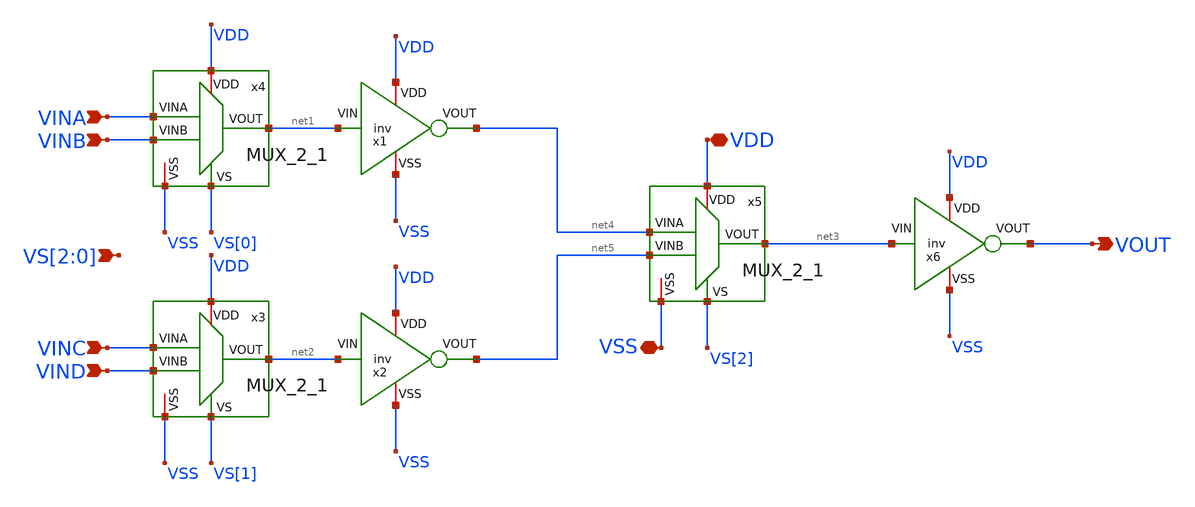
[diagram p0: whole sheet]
** sch_path: Custom_std_cells/MUX_4_1.sch
**.subckt MUX_4_1 VOUT VDD VSS VINA VINB VINC VIND VS[2],VS[1],VS[0]
*.opin VOUT
*.iopin VDD
*.iopin VSS
*.ipin VINA
*.ipin VINB
*.ipin VINC
*.ipin VIND
*.ipin VS[2],VS[1],VS[0]
x3 VDD VINC net2 VS[1] VIND VSS MUX_2_1
x4 VDD VINA net1 VS[0] VINB VSS MUX_2_1
x5 VDD net4 net3 VS[2] net5 VSS MUX_2_1
x1 VDD net4 net1 VSS inv
x2 VDD net5 net2 VSS inv
x6 VDD VOUT net3 VSS inv
**.ends
.end
